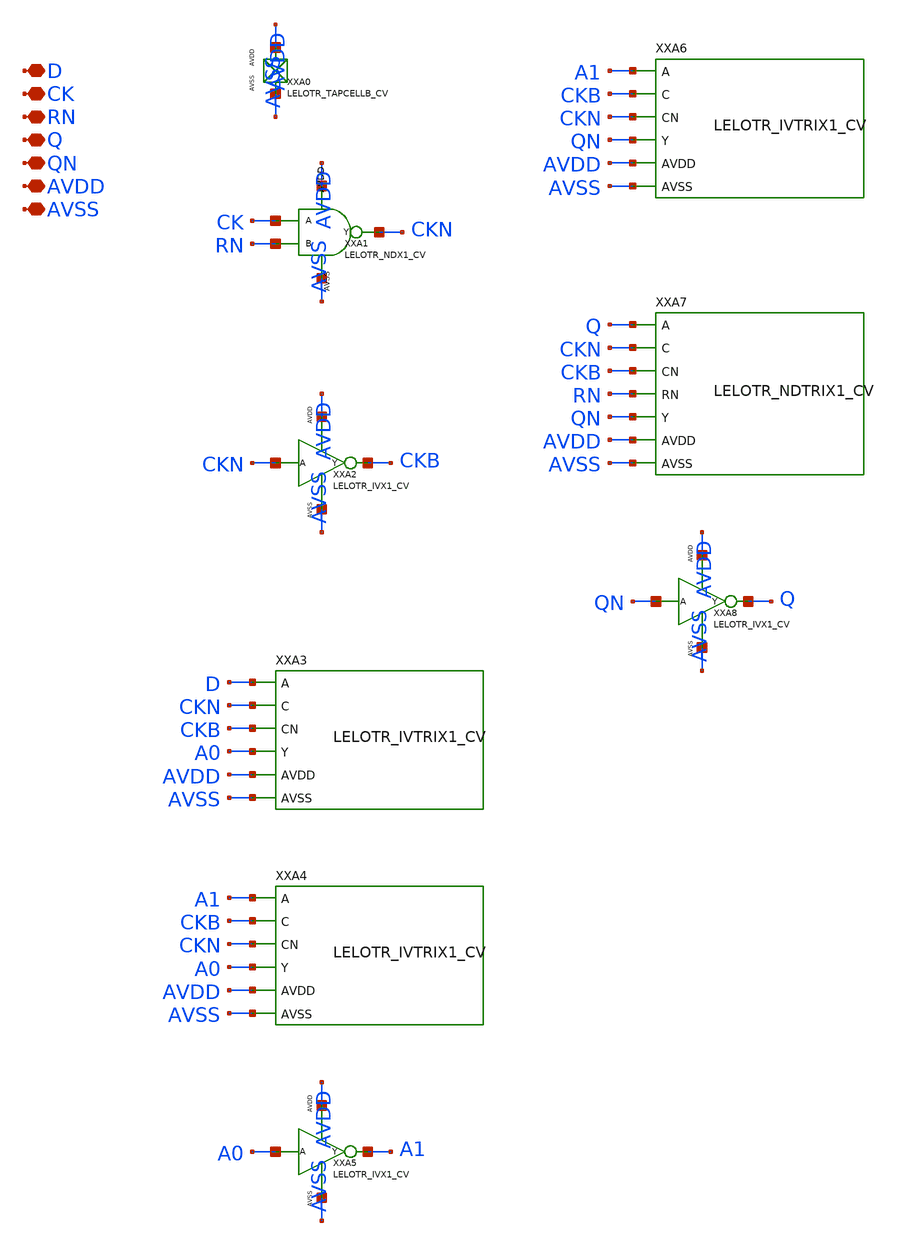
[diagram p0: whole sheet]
** sch_path: design/LELO_TR_GF180MCUD/LELOTR_DFRNQNX1_CV.sch
**.subckt LELOTR_DFRNQNX1_CV D CK RN Q QN AVDD AVSS
*.iopin D
*.iopin CK
*.iopin RN
*.iopin Q
*.iopin QN
*.iopin AVDD
*.iopin AVSS
XXA0 AVDD AVSS LELOTR_TAPCELLB_CV xoffset=0 yoffset=0 angle=0
XXA1 CK RN CKN AVDD AVSS LELOTR_NDX1_CV
XXA2 CKN CKB AVDD AVSS LELOTR_IVX1_CV
XXA3 D CKN CKB A0 AVDD AVSS LELOTR_IVTRIX1_CV
XXA4 A1 CKB CKN A0 AVDD AVSS LELOTR_IVTRIX1_CV
XXA5 A0 A1 AVDD AVSS LELOTR_IVX1_CV
XXA6 A1 CKB CKN QN AVDD AVSS LELOTR_IVTRIX1_CV
XXA7 Q CKN CKB RN QN AVDD AVSS LELOTR_NDTRIX1_CV
XXA8 QN Q AVDD AVSS LELOTR_IVX1_CV
**.ends
.end
